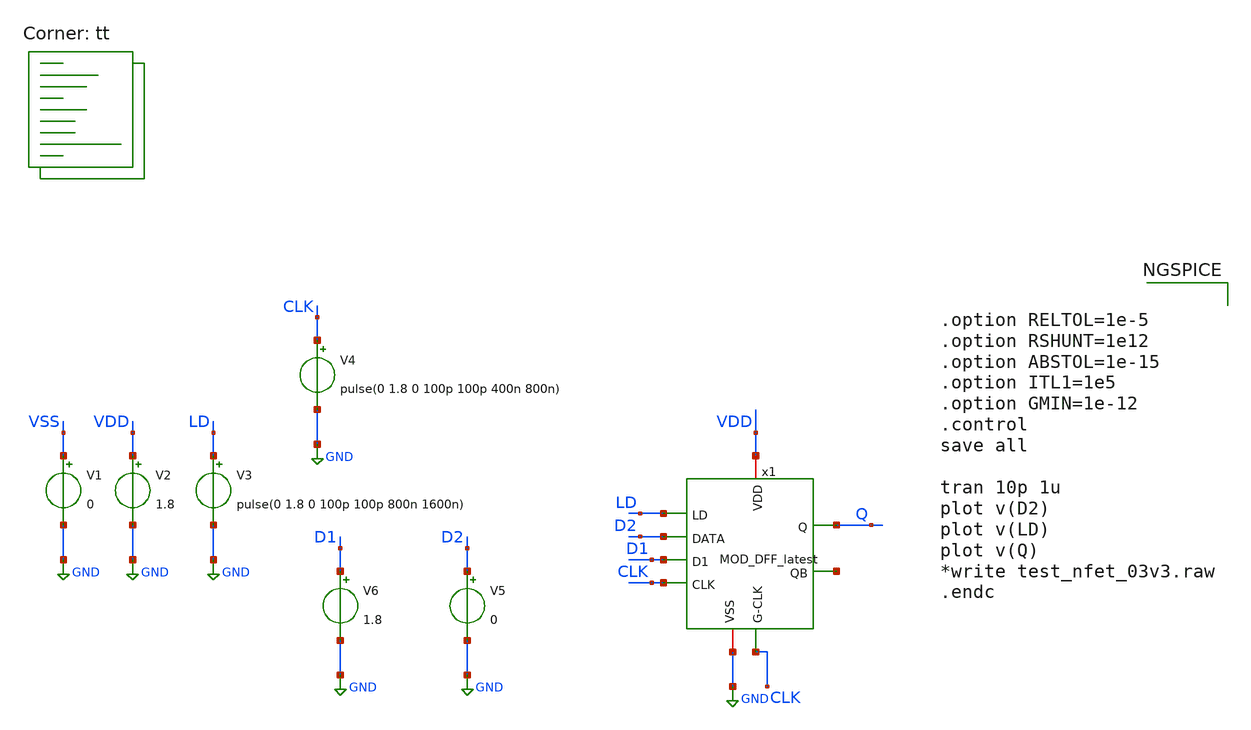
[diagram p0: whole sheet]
** sch_path: Xschem/PLL_TOP_Schematics/mod_DFF_tb.sch
**.subckt mod_DFF_tb
V1 VSS GND 0
V2 VDD GND 1.8
V3 LD GND pulse(0 1.8 0 100p 100p 800n 1600n)
V4 CLK GND pulse(0 1.8 0 100p 100p 400n 800n)
V5 D2 GND 0
V6 D1 GND 1.8
x1 VDD LD D2 Q net1 D1 GND CLK CLK MOD_DFF_latest
**** begin user architecture code


.option RELTOL=1e-5
.option RSHUNT=1e12
.option ABSTOL=1e-15
.option ITL1=1e5
.option GMIN=1e-12
.control
save all

tran 10p 1u
plot v(D2)
plot v(LD)
plot v(Q)
*write test_nfet_03v3.raw
.endc


.lib $::SKYWATER_MODELS/sky130.lib.spice tt
**** end user architecture code
**.ends
.GLOBAL GND
.end
